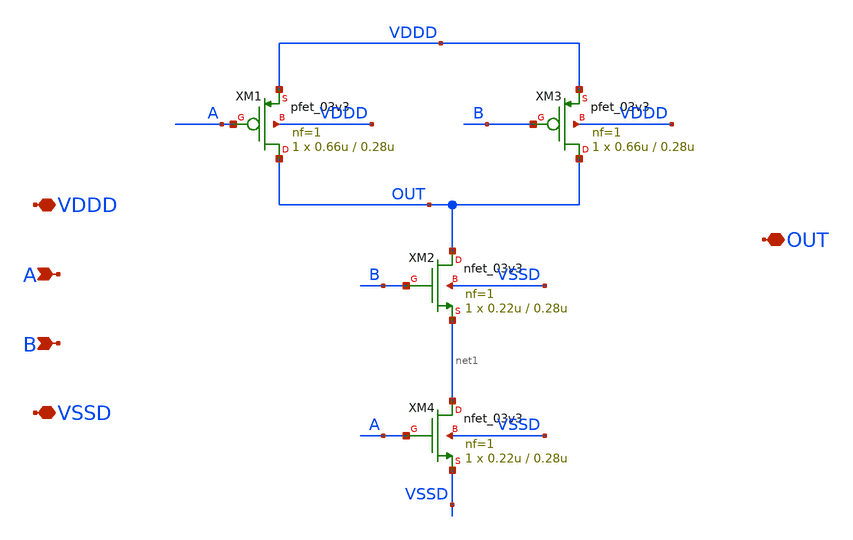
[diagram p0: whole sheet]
** sch_path: SAR_ADC/blocks/SAR_logic/nand_2_1x.sch
**.subckt nand_2_1x A B VDDD VSSD OUT
*.ipin A
*.ipin B
*.iopin VDDD
*.iopin VSSD
*.iopin OUT
XM1 OUT A VDDD VDDD pfet_03v3 L=0.28u W=0.66u nf=1 ad='int((nf+1)/2) * W/nf * 0.18u' as='int((nf+2)/2) * W/nf * 0.18u'
+ pd='2*int((nf+1)/2) * (W/nf + 0.18u)' ps='2*int((nf+2)/2) * (W/nf + 0.18u)' nrd='0.18u / W' nrs='0.18u / W'
+ sa=0 sb=0 sd=0 m=1 par=1
XM2 OUT B net1 VSSD nfet_03v3 L=0.28u W=0.22u nf=1 ad='int((nf+1)/2) * W/nf * 0.18u' as='int((nf+2)/2) * W/nf * 0.18u'
+ pd='2*int((nf+1)/2) * (W/nf + 0.18u)' ps='2*int((nf+2)/2) * (W/nf + 0.18u)' nrd='0.18u / W' nrs='0.18u / W'
+ sa=0 sb=0 sd=0 m=1 par=1
XM3 OUT B VDDD VDDD pfet_03v3 L=0.28u W=0.66u nf=1 ad='int((nf+1)/2) * W/nf * 0.18u' as='int((nf+2)/2) * W/nf * 0.18u'
+ pd='2*int((nf+1)/2) * (W/nf + 0.18u)' ps='2*int((nf+2)/2) * (W/nf + 0.18u)' nrd='0.18u / W' nrs='0.18u / W'
+ sa=0 sb=0 sd=0 m=1 par=1
XM4 net1 A VSSD VSSD nfet_03v3 L=0.28u W=0.22u nf=1 ad='int((nf+1)/2) * W/nf * 0.18u' as='int((nf+2)/2) * W/nf * 0.18u'
+ pd='2*int((nf+1)/2) * (W/nf + 0.18u)' ps='2*int((nf+2)/2) * (W/nf + 0.18u)' nrd='0.18u / W' nrs='0.18u / W'
+ sa=0 sb=0 sd=0 m=1 par=1
**.ends
.end
